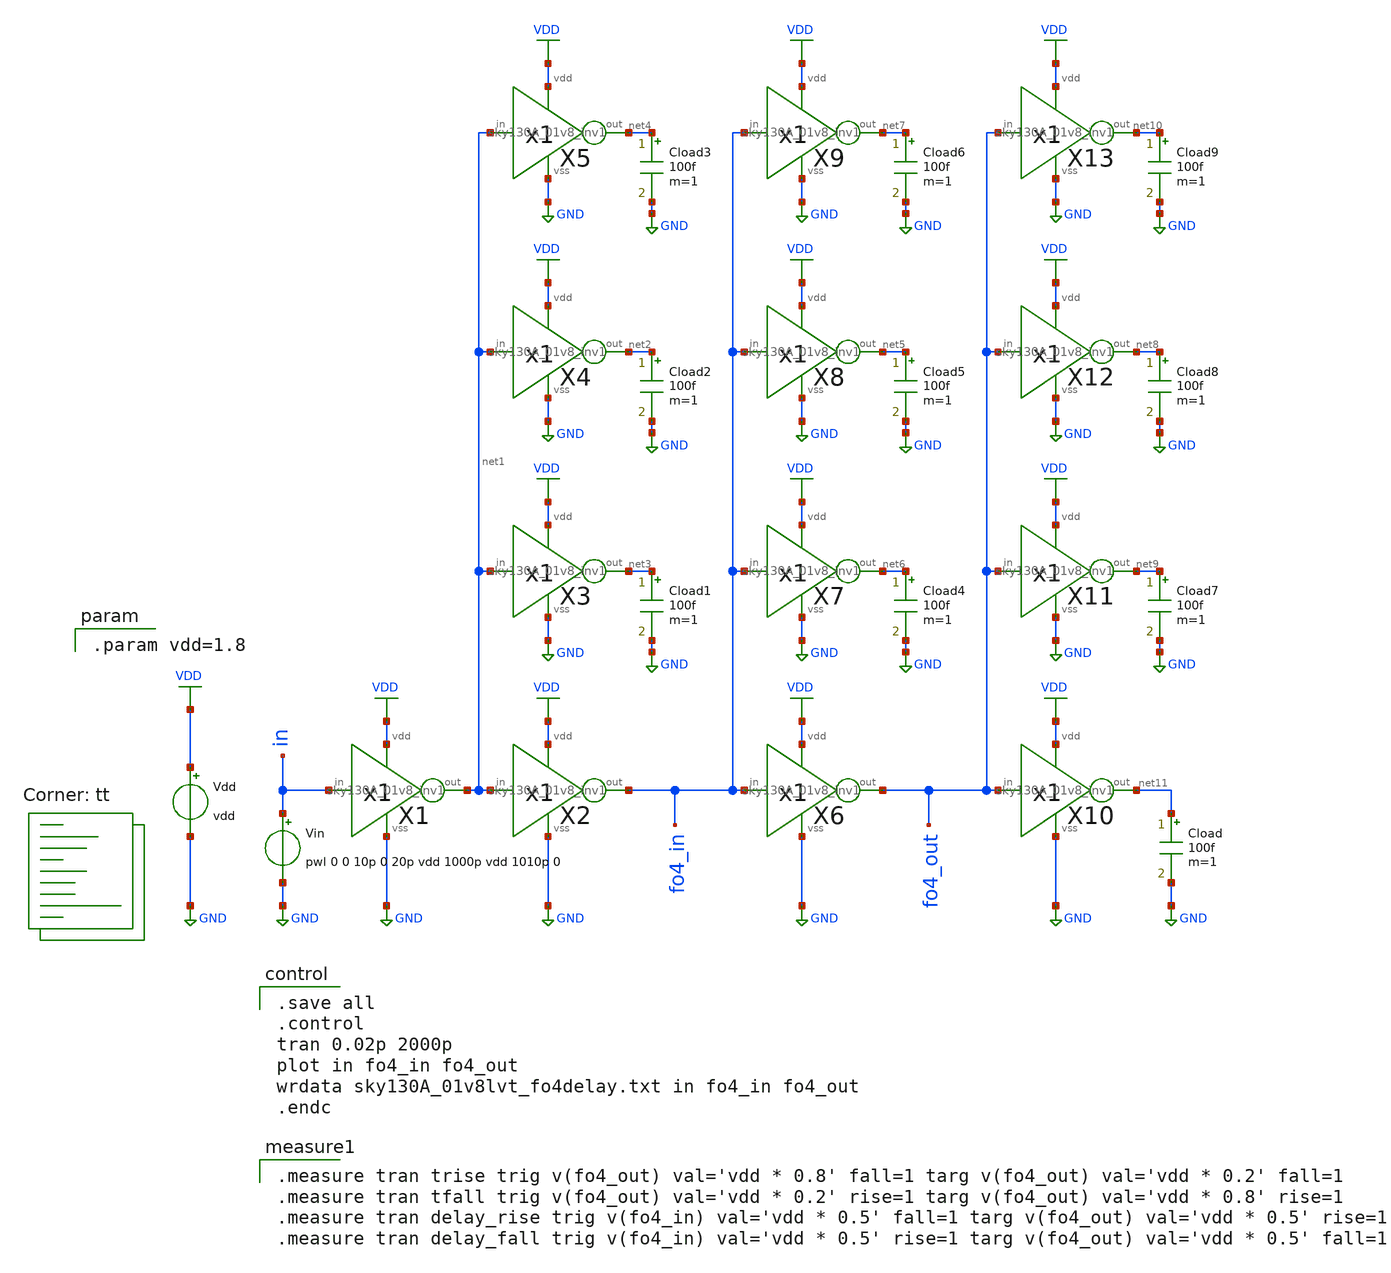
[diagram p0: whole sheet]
** sch_path: xschem/Logic/sky130A_01v8_fo4delay.sch
* Copyright 2021 Stefan Frederik Schippers
* Licensed under the Apache License, Version 2.0 (the "License");
* you may not use this file except in compliance with the License.
* You may obtain a copy of the License at
* https://www.apache.org/licenses/LICENSE-2.0
* Unless required by applicable law or agreed to in writing, software
* distributed under the License is distributed on an "AS IS" BASIS,
* WITHOUT WARRANTIES OR CONDITIONS OF ANY KIND, either express or implied.
* See the License for the specific language governing permissions and
* limitations under the License.
**.subckt sky130A_01v8_fo4delay
Vdd VDD GND vdd
Vin in GND pwl 0 0 10p 0 20p vdd 1000p vdd 1010p 0
Cload net11 GND 100f m=1
X1 VDD GND net1 in sky130A_01v8_inv1
Cload1 net3 GND 100f m=1
Cload2 net2 GND 100f m=1
Cload3 net4 GND 100f m=1
Cload4 net6 GND 100f m=1
Cload5 net5 GND 100f m=1
Cload6 net7 GND 100f m=1
Cload7 net9 GND 100f m=1
Cload8 net8 GND 100f m=1
Cload9 net10 GND 100f m=1
X2 VDD GND fo4_in net1 sky130A_01v8_inv1
X3 VDD GND net3 net1 sky130A_01v8_inv1
X4 VDD GND net2 net1 sky130A_01v8_inv1
X5 VDD GND net4 net1 sky130A_01v8_inv1
X6 VDD GND fo4_out fo4_in sky130A_01v8_inv1
X7 VDD GND net6 fo4_in sky130A_01v8_inv1
X8 VDD GND net5 fo4_in sky130A_01v8_inv1
X9 VDD GND net7 fo4_in sky130A_01v8_inv1
X10 VDD GND net11 fo4_out sky130A_01v8_inv1
X11 VDD GND net9 fo4_out sky130A_01v8_inv1
X12 VDD GND net8 fo4_out sky130A_01v8_inv1
X13 VDD GND net10 fo4_out sky130A_01v8_inv1
**** begin user architecture code
.lib $::SKYWATER_MODELS/sky130.lib.spice tt

.save all
.control
tran 0.02p 2000p
plot in fo4_in fo4_out
wrdata sky130A_01v8lvt_fo4delay.txt in fo4_in fo4_out
.endc


.param vdd=1.8


.measure tran trise trig v(fo4_out) val='vdd * 0.8' fall=1 targ v(fo4_out) val='vdd * 0.2' fall=1
.measure tran tfall trig v(fo4_out) val='vdd * 0.2' rise=1 targ v(fo4_out) val='vdd * 0.8' rise=1
.measure tran delay_rise trig v(fo4_in) val='vdd * 0.5' fall=1 targ v(fo4_out) val='vdd * 0.5' rise=1
.measure tran delay_fall trig v(fo4_in) val='vdd * 0.5' rise=1 targ v(fo4_out) val='vdd * 0.5' fall=1

**** end user architecture code
**.ends

* expanding   symbol:  symbols/sky130A_01v8_inv1.sym # of pins=4
** sym_path: xschem/symbols/sky130A_01v8_inv1.sym
** sch_path: xschem/symbols/sky130A_01v8_inv1.sch
.subckt sky130A_01v8_inv1 vdd vss out in
*.iopin vdd
*.iopin vss
*.ipin in
*.opin out
XM11 out in vdd vdd sky130_fd_pr__pfet_01v8 L=0.15 W=2 nf=1 ad='int((nf+1)/2) * W/nf * 0.29' as='int((nf+2)/2) * W/nf * 0.29'
+ pd='2*int((nf+1)/2) * (W/nf + 0.29)' ps='2*int((nf+2)/2) * (W/nf + 0.29)' nrd='0.29 / W' nrs='0.29 / W'
+ sa=0 sb=0 sd=0 mult=1 m=1
XM2 out in vss vss sky130_fd_pr__nfet_01v8 L=0.15 W=1 nf=1 ad='int((1 + 1)/2) * 1 / 1 * 0.29' as='int((1 + 2)/2) * 1 / 1 * 0.29'
+ pd='2*int((1 + 1)/2) * (1 / 1 + 0.29)' ps='2*int((1 + 2)/2) * (1 / 1 + 0.29)' nrd='0.29 / 1 ' nrs='0.29 / 1 '
+ sa=0 sb=0 sd=0 mult=1 m=1
.ends

.GLOBAL VDD
.GLOBAL GND
.end
